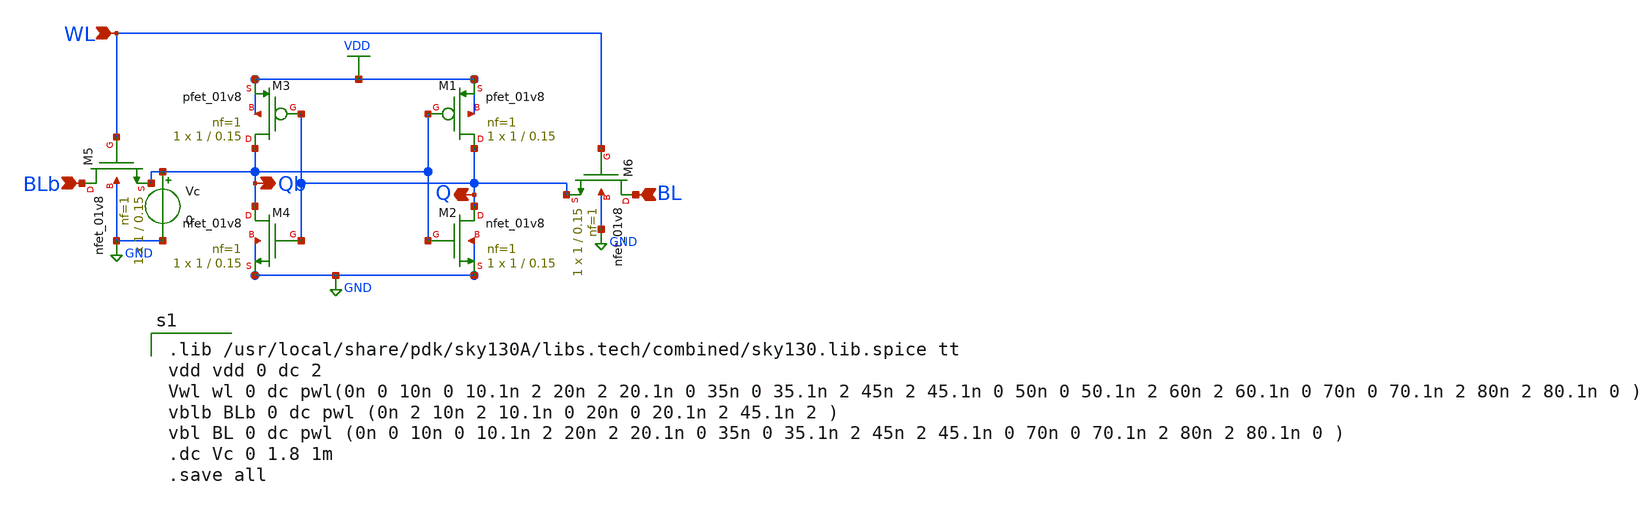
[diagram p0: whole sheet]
** sch_path: Circuit Files/circuits/circuits/ROM6T.sch
**.subckt ROM6T WL BLb BL Q Qb
*.ipin WL
*.ipin BLb
*.ipin BL
*.opin Q
*.opin Qb
XM1 Q Qb VDD VDD sky130_fd_pr__pfet_01v8 L=0.15 W=1 nf=1 ad='int((nf+1)/2) * W/nf * 0.29' as='int((nf+2)/2) * W/nf * 0.29'
+ pd='2*int((nf+1)/2) * (W/nf + 0.29)' ps='2*int((nf+2)/2) * (W/nf + 0.29)' nrd='0.29 / W' nrs='0.29 / W'
+ sa=0 sb=0 sd=0 mult=1 m=1
XM2 Q Qb GND GND sky130_fd_pr__nfet_01v8 L=0.15 W=1 nf=1 ad='int((nf+1)/2) * W/nf * 0.29' as='int((nf+2)/2) * W/nf * 0.29'
+ pd='2*int((nf+1)/2) * (W/nf + 0.29)' ps='2*int((nf+2)/2) * (W/nf + 0.29)' nrd='0.29 / W' nrs='0.29 / W'
+ sa=0 sb=0 sd=0 mult=1 m=1
XM3 Qb Q VDD VDD sky130_fd_pr__pfet_01v8 L=0.15 W=1 nf=1 ad='int((nf+1)/2) * W/nf * 0.29' as='int((nf+2)/2) * W/nf * 0.29'
+ pd='2*int((nf+1)/2) * (W/nf + 0.29)' ps='2*int((nf+2)/2) * (W/nf + 0.29)' nrd='0.29 / W' nrs='0.29 / W'
+ sa=0 sb=0 sd=0 mult=1 m=1
XM4 Qb Q GND GND sky130_fd_pr__nfet_01v8 L=0.15 W=1 nf=1 ad='int((nf+1)/2) * W/nf * 0.29' as='int((nf+2)/2) * W/nf * 0.29'
+ pd='2*int((nf+1)/2) * (W/nf + 0.29)' ps='2*int((nf+2)/2) * (W/nf + 0.29)' nrd='0.29 / W' nrs='0.29 / W'
+ sa=0 sb=0 sd=0 mult=1 m=1
XM5 BLb WL Qb GND sky130_fd_pr__nfet_01v8 L=0.15 W=1 nf=1 ad='int((nf+1)/2) * W/nf * 0.29' as='int((nf+2)/2) * W/nf * 0.29'
+ pd='2*int((nf+1)/2) * (W/nf + 0.29)' ps='2*int((nf+2)/2) * (W/nf + 0.29)' nrd='0.29 / W' nrs='0.29 / W'
+ sa=0 sb=0 sd=0 mult=1 m=1
XM6 BL WL Q GND sky130_fd_pr__nfet_01v8 L=0.15 W=1 nf=1 ad='int((nf+1)/2) * W/nf * 0.29' as='int((nf+2)/2) * W/nf * 0.29'
+ pd='2*int((nf+1)/2) * (W/nf + 0.29)' ps='2*int((nf+2)/2) * (W/nf + 0.29)' nrd='0.29 / W' nrs='0.29 / W'
+ sa=0 sb=0 sd=0 mult=1 m=1
Vc Qb GND 0
**** begin user architecture code

.lib /usr/local/share/pdk/sky130A/libs.tech/combined/sky130.lib.spice tt
vdd vdd 0 dc 2
Vwl wl 0 dc pwl(0n 0 10n 0 10.1n 2 20n 2 20.1n 0 35n 0 35.1n 2 45n 2 45.1n 0 50n 0 50.1n 2 60n 2
+ 60.1n 0 70n 0 70.1n 2 80n 2 80.1n 0 )
vblb BLb 0 dc pwl (0n 2 10n 2 10.1n 0 20n 0 20.1n 2 45.1n 2 )
vbl BL 0 dc pwl (0n 0 10n 0 10.1n 2 20n 2 20.1n 0 35n 0 35.1n 2 45n 2 45.1n 0 70n 0 70.1n 2 80n 2
+ 80.1n 0 )
.dc Vc 0 1.8 1m
.save all


**** end user architecture code
**.ends
.GLOBAL GND
.GLOBAL VDD
.end
